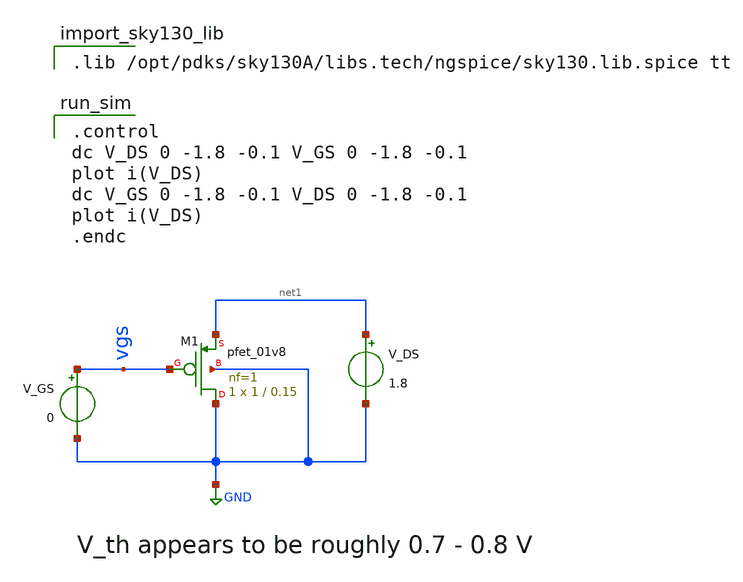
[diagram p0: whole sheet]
** sch_path: xschem/pfet_characterization.sch
**.subckt pfet_characterization
V_GS vgs GND 0
V_DS net1 GND 1.8
XM1 GND vgs net1 GND sky130_fd_pr__pfet_01v8 L=0.15 W=1 nf=1 ad='int((nf+1)/2) * W/nf * 0.29' as='int((nf+2)/2) * W/nf * 0.29'
+ pd='2*int((nf+1)/2) * (W/nf + 0.29)' ps='2*int((nf+2)/2) * (W/nf + 0.29)' nrd='0.29 / W' nrs='0.29 / W'
+ sa=0 sb=0 sd=0 mult=1 m=1
**** begin user architecture code

.lib /opt/pdks/sky130A/libs.tech/ngspice/sky130.lib.spice tt


.control
dc V_DS 0 -1.8 -0.1 V_GS 0 -1.8 -0.1
plot i(V_DS)
dc V_GS 0 -1.8 -0.1 V_DS 0 -1.8 -0.1
plot i(V_DS)
.endc

**** end user architecture code
**.ends
.GLOBAL GND
.end
